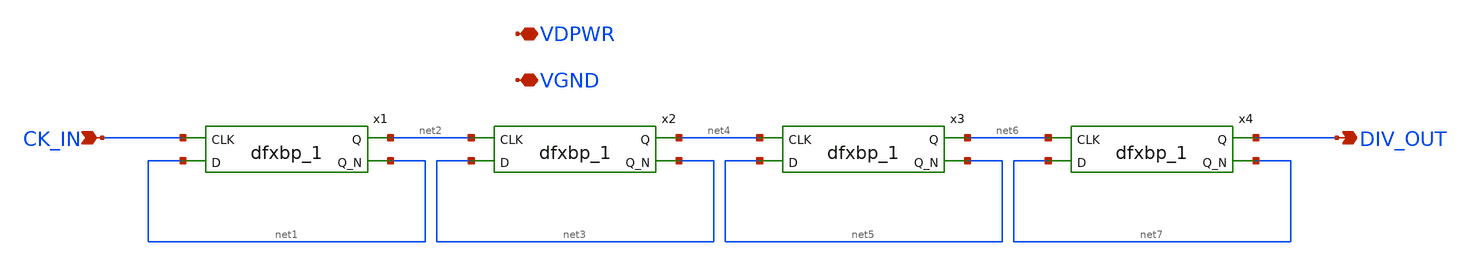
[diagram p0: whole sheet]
** sch_path: designs/bgr_ldo/ldo/div16_core.sch
**.subckt div16_core CK_IN DIV_OUT VDPWR VGND
*.ipin CK_IN
*.opin DIV_OUT
*.iopin VDPWR
*.iopin VGND
x1 CK_IN net1 VGND VGND VDPWR VDPWR net2 net1 sky130_fd_sc_hd__dfxbp_1
x2 net2 net3 VGND VGND VDPWR VDPWR net4 net3 sky130_fd_sc_hd__dfxbp_1
x3 net4 net5 VGND VGND VDPWR VDPWR net6 net5 sky130_fd_sc_hd__dfxbp_1
x4 net6 net7 VGND VGND VDPWR VDPWR DIV_OUT net7 sky130_fd_sc_hd__dfxbp_1
**.ends
.end
